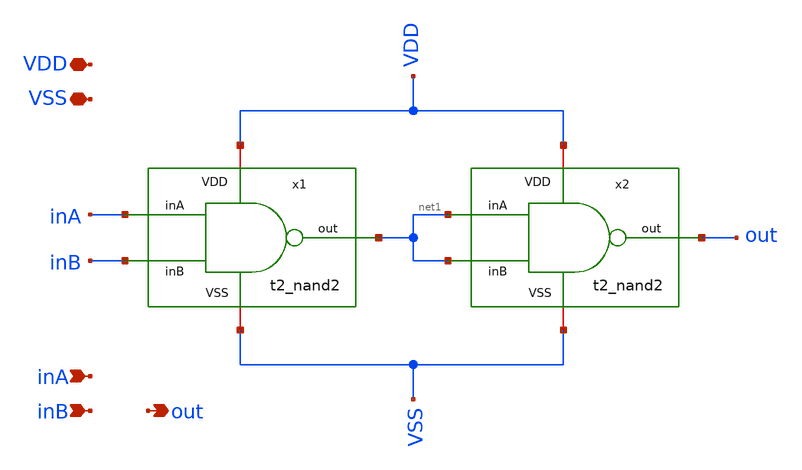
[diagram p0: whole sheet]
** sch_path: Team Designs/Team 2 Design/design_data/xschem/t2_and2.sch
**.subckt t2_and2 VSS inA inB out VDD
*.iopin VSS
*.ipin inA
*.ipin inB
*.opin out
*.iopin VDD
x1 VDD inA inB net1 VSS t2_nand2
x2 VDD net1 net1 out VSS t2_nand2
**.ends

* expanding   symbol:  t2_nand2.sym # of pins=5
** sym_path: Team 2 Design/design_data/xschem/t2_nand2.sym
** sch_path: Team 2 Design/design_data/xschem/t2_nand2.sch
.subckt t2_nand2 VDD inA inB out VSS
*.iopin VSS
*.ipin inA
*.ipin inB
*.opin out
*.iopin VDD
XM1 out inA VDD VDD sg13_lv_pmos w=1u l=0.45u ng=1 m=1 mm_ok=1
XM2 out inB VDD VDD sg13_lv_pmos w=1u l=0.45u ng=1 m=1 mm_ok=1
XM3 out inB net1 VSS sg13_lv_nmos w=0.5u l=0.45u ng=1 m=1 mm_ok=1
XM4 net1 inA VSS VSS sg13_lv_nmos w=0.5u l=0.45u ng=1 m=1 mm_ok=1
.ends

.end
